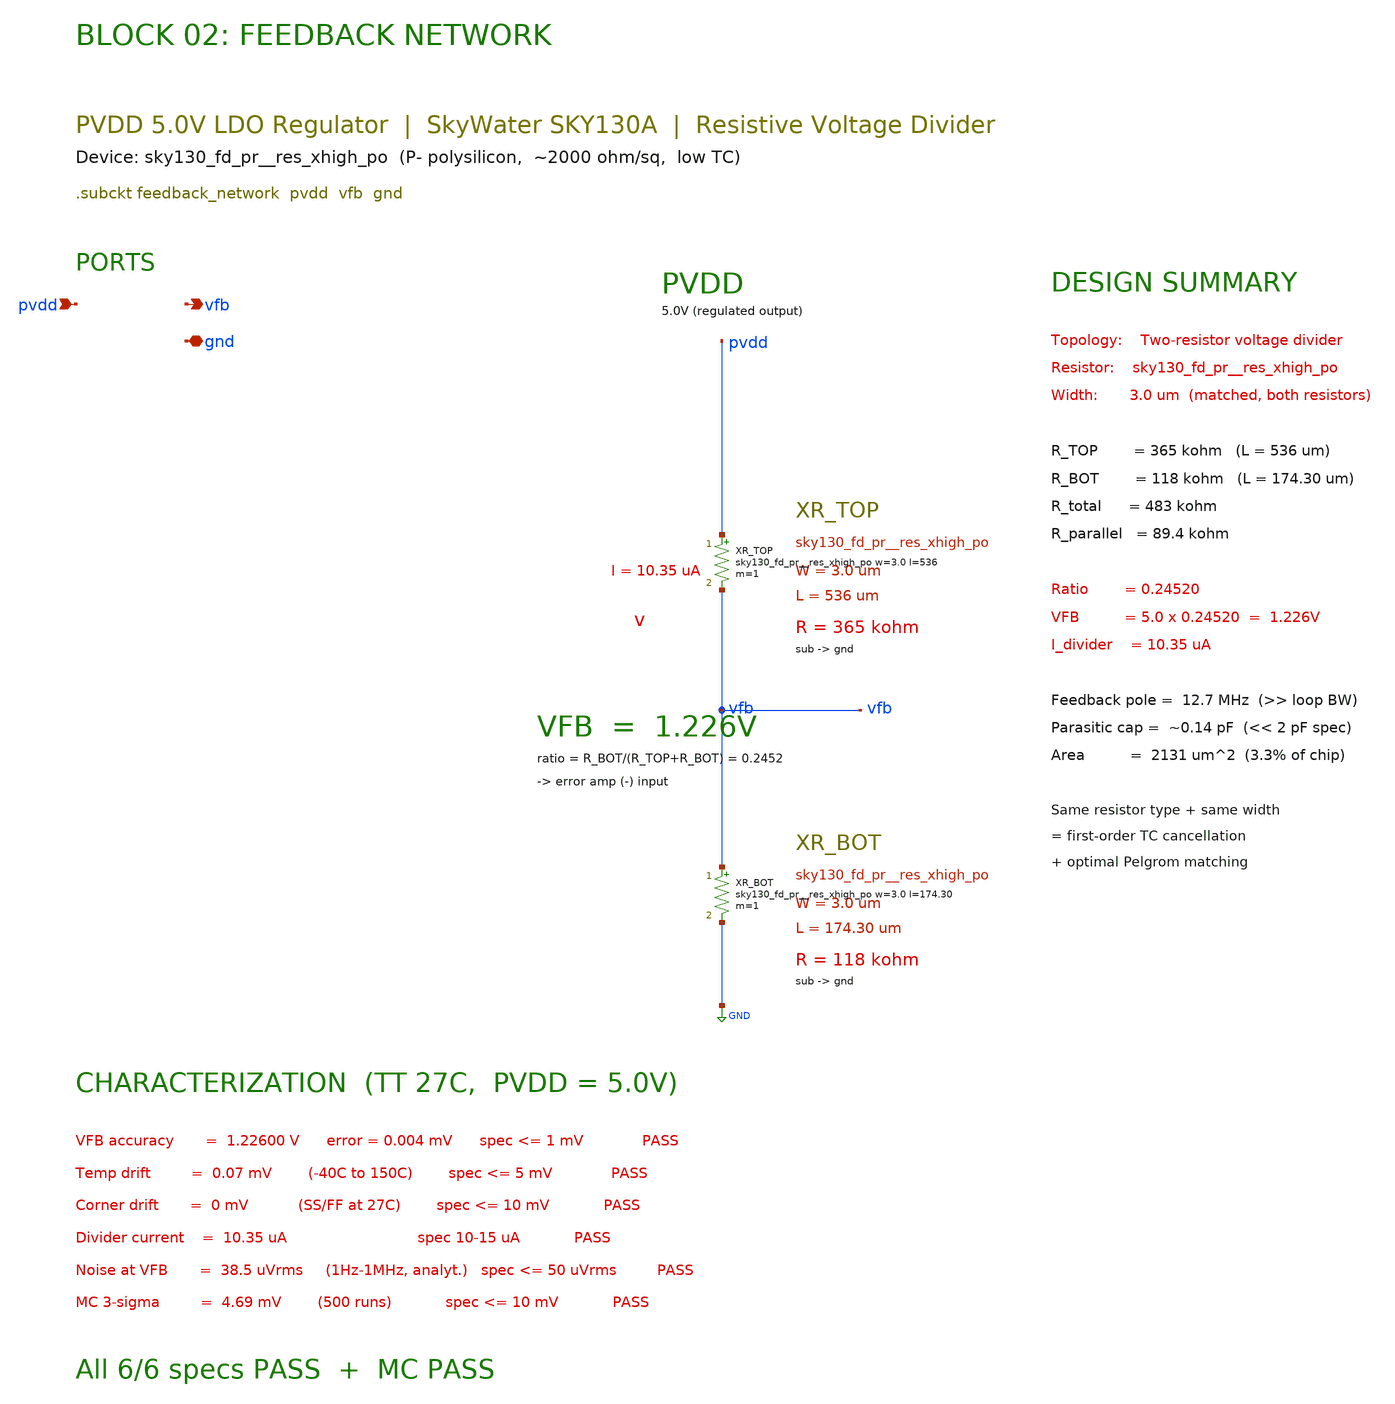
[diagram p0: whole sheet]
** sch_path: pvdd_regulator/02_feedback_network/feedback_network.sch
**.subckt feedback_network pvdd vfb gnd
*.ipin pvdd
*.opin vfb
*.iopin gnd
XR_TOP pvdd vfb sky130_fd_pr__res_xhigh_po w=3.0 l=536 m=1
XR_BOT vfb GND sky130_fd_pr__res_xhigh_po w=3.0 l=174.30 m=1
**.ends
.GLOBAL GND
.end
